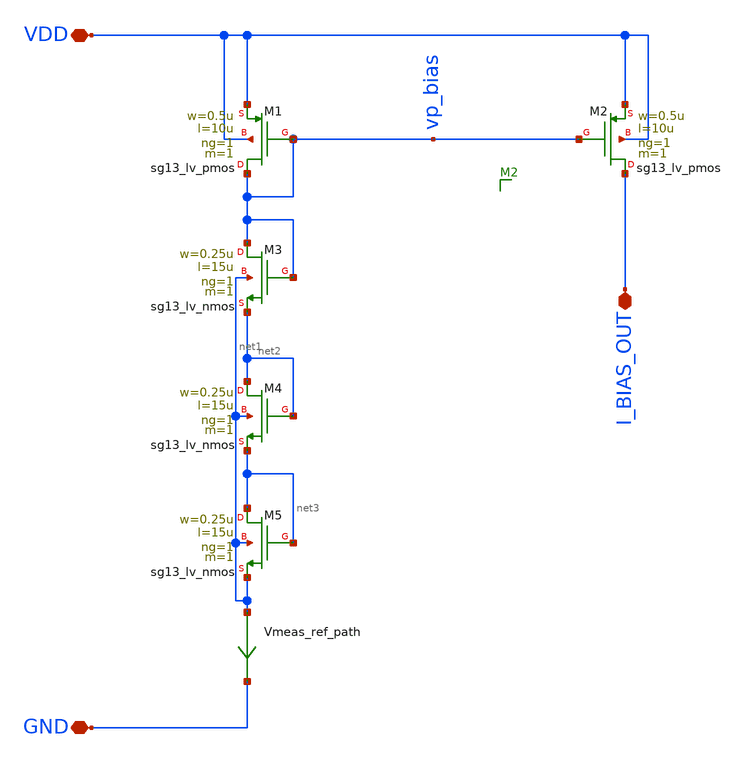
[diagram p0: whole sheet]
** sch_path: osc_bias.sch
**.subckt osc_bias VDD GND I_BIAS_OUT
*.iopin VDD
*.iopin GND
*.iopin I_BIAS_OUT
XM1 vp_bias vp_bias VDD VDD sg13_lv_pmos w=0.5u l=10u ng=1 m=1 mm_ok=1
XM3 vp_bias vp_bias net2 net1 sg13_lv_nmos w=0.25u l=15u ng=1 m=1 mm_ok=1
XM4 net2 net2 net3 net1 sg13_lv_nmos w=0.25u l=15u ng=1 m=1 mm_ok=1
XM5 net3 net3 net1 net1 sg13_lv_nmos w=0.25u l=15u ng=1 m=1 mm_ok=1
XM2 I_BIAS_OUT vp_bias VDD VDD sg13_lv_pmos w=0.5u l=10u ng=1 m=1 mm_ok=1
Vmeas_ref_path net1 GND 0
.save i(vmeas_ref_path)
**.ends
.end
